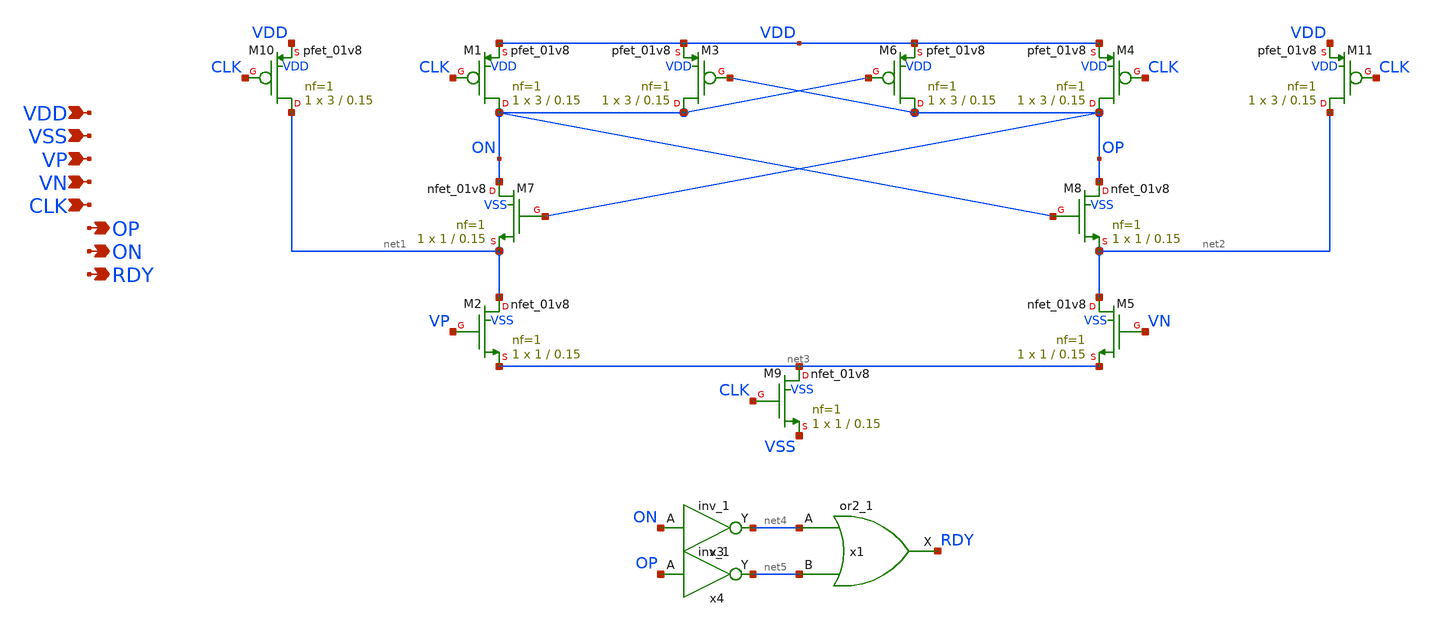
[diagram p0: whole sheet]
** sch_path: xschem/cmp.sch
**.subckt cmp VDD VSS VP VN OP ON RDY CLK
*.ipin VDD
*.ipin VSS
*.ipin VP
*.ipin VN
*.opin OP
*.opin ON
*.opin RDY
*.ipin CLK
XM1 ON CLK VDD VDD sky130_fd_pr__pfet_01v8 L=0.15 W=3 nf=1 ad='int((nf+1)/2) * W/nf * 0.29' as='int((nf+2)/2) * W/nf * 0.29'
+ pd='2*int((nf+1)/2) * (W/nf + 0.29)' ps='2*int((nf+2)/2) * (W/nf + 0.29)' nrd='0.29 / W' nrs='0.29 / W'
+ sa=0 sb=0 sd=0 mult=1 m=1
XM2 net1 VP net3 VSS sky130_fd_pr__nfet_01v8 L=0.15 W=1 nf=1 ad='int((nf+1)/2) * W/nf * 0.29' as='int((nf+2)/2) * W/nf * 0.29'
+ pd='2*int((nf+1)/2) * (W/nf + 0.29)' ps='2*int((nf+2)/2) * (W/nf + 0.29)' nrd='0.29 / W' nrs='0.29 / W'
+ sa=0 sb=0 sd=0 mult=1 m=1
XM3 ON OP VDD VDD sky130_fd_pr__pfet_01v8 L=0.15 W=3 nf=1 ad='int((nf+1)/2) * W/nf * 0.29' as='int((nf+2)/2) * W/nf * 0.29'
+ pd='2*int((nf+1)/2) * (W/nf + 0.29)' ps='2*int((nf+2)/2) * (W/nf + 0.29)' nrd='0.29 / W' nrs='0.29 / W'
+ sa=0 sb=0 sd=0 mult=1 m=1
XM4 OP CLK VDD VDD sky130_fd_pr__pfet_01v8 L=0.15 W=3 nf=1 ad='int((nf+1)/2) * W/nf * 0.29' as='int((nf+2)/2) * W/nf * 0.29'
+ pd='2*int((nf+1)/2) * (W/nf + 0.29)' ps='2*int((nf+2)/2) * (W/nf + 0.29)' nrd='0.29 / W' nrs='0.29 / W'
+ sa=0 sb=0 sd=0 mult=1 m=1
XM5 net2 VN net3 VSS sky130_fd_pr__nfet_01v8 L=0.15 W=1 nf=1 ad='int((nf+1)/2) * W/nf * 0.29' as='int((nf+2)/2) * W/nf * 0.29'
+ pd='2*int((nf+1)/2) * (W/nf + 0.29)' ps='2*int((nf+2)/2) * (W/nf + 0.29)' nrd='0.29 / W' nrs='0.29 / W'
+ sa=0 sb=0 sd=0 mult=1 m=1
XM6 OP ON VDD VDD sky130_fd_pr__pfet_01v8 L=0.15 W=3 nf=1 ad='int((nf+1)/2) * W/nf * 0.29' as='int((nf+2)/2) * W/nf * 0.29'
+ pd='2*int((nf+1)/2) * (W/nf + 0.29)' ps='2*int((nf+2)/2) * (W/nf + 0.29)' nrd='0.29 / W' nrs='0.29 / W'
+ sa=0 sb=0 sd=0 mult=1 m=1
XM7 ON OP net1 VSS sky130_fd_pr__nfet_01v8 L=0.15 W=1 nf=1 ad='int((nf+1)/2) * W/nf * 0.29' as='int((nf+2)/2) * W/nf * 0.29'
+ pd='2*int((nf+1)/2) * (W/nf + 0.29)' ps='2*int((nf+2)/2) * (W/nf + 0.29)' nrd='0.29 / W' nrs='0.29 / W'
+ sa=0 sb=0 sd=0 mult=1 m=1
XM8 OP ON net2 VSS sky130_fd_pr__nfet_01v8 L=0.15 W=1 nf=1 ad='int((nf+1)/2) * W/nf * 0.29' as='int((nf+2)/2) * W/nf * 0.29'
+ pd='2*int((nf+1)/2) * (W/nf + 0.29)' ps='2*int((nf+2)/2) * (W/nf + 0.29)' nrd='0.29 / W' nrs='0.29 / W'
+ sa=0 sb=0 sd=0 mult=1 m=1
XM9 net3 CLK VSS VSS sky130_fd_pr__nfet_01v8 L=0.15 W=1 nf=1 ad='int((nf+1)/2) * W/nf * 0.29' as='int((nf+2)/2) * W/nf * 0.29'
+ pd='2*int((nf+1)/2) * (W/nf + 0.29)' ps='2*int((nf+2)/2) * (W/nf + 0.29)' nrd='0.29 / W' nrs='0.29 / W'
+ sa=0 sb=0 sd=0 mult=1 m=1
XM10 net1 CLK VDD VDD sky130_fd_pr__pfet_01v8 L=0.15 W=3 nf=1 ad='int((nf+1)/2) * W/nf * 0.29' as='int((nf+2)/2) * W/nf * 0.29'
+ pd='2*int((nf+1)/2) * (W/nf + 0.29)' ps='2*int((nf+2)/2) * (W/nf + 0.29)' nrd='0.29 / W' nrs='0.29 / W'
+ sa=0 sb=0 sd=0 mult=1 m=1
XM11 net2 CLK VDD VDD sky130_fd_pr__pfet_01v8 L=0.15 W=3 nf=1 ad='int((nf+1)/2) * W/nf * 0.29' as='int((nf+2)/2) * W/nf * 0.29'
+ pd='2*int((nf+1)/2) * (W/nf + 0.29)' ps='2*int((nf+2)/2) * (W/nf + 0.29)' nrd='0.29 / W' nrs='0.29 / W'
+ sa=0 sb=0 sd=0 mult=1 m=1
x1 net4 net5 VSS VSS VDD VDD RDY sky130_fd_sc_hd__or2_1
x3 ON VSS VSS VDD VDD net4 sky130_fd_sc_hd__inv_1
x4 OP VSS VSS VDD VDD net5 sky130_fd_sc_hd__inv_1
**.ends
.end
